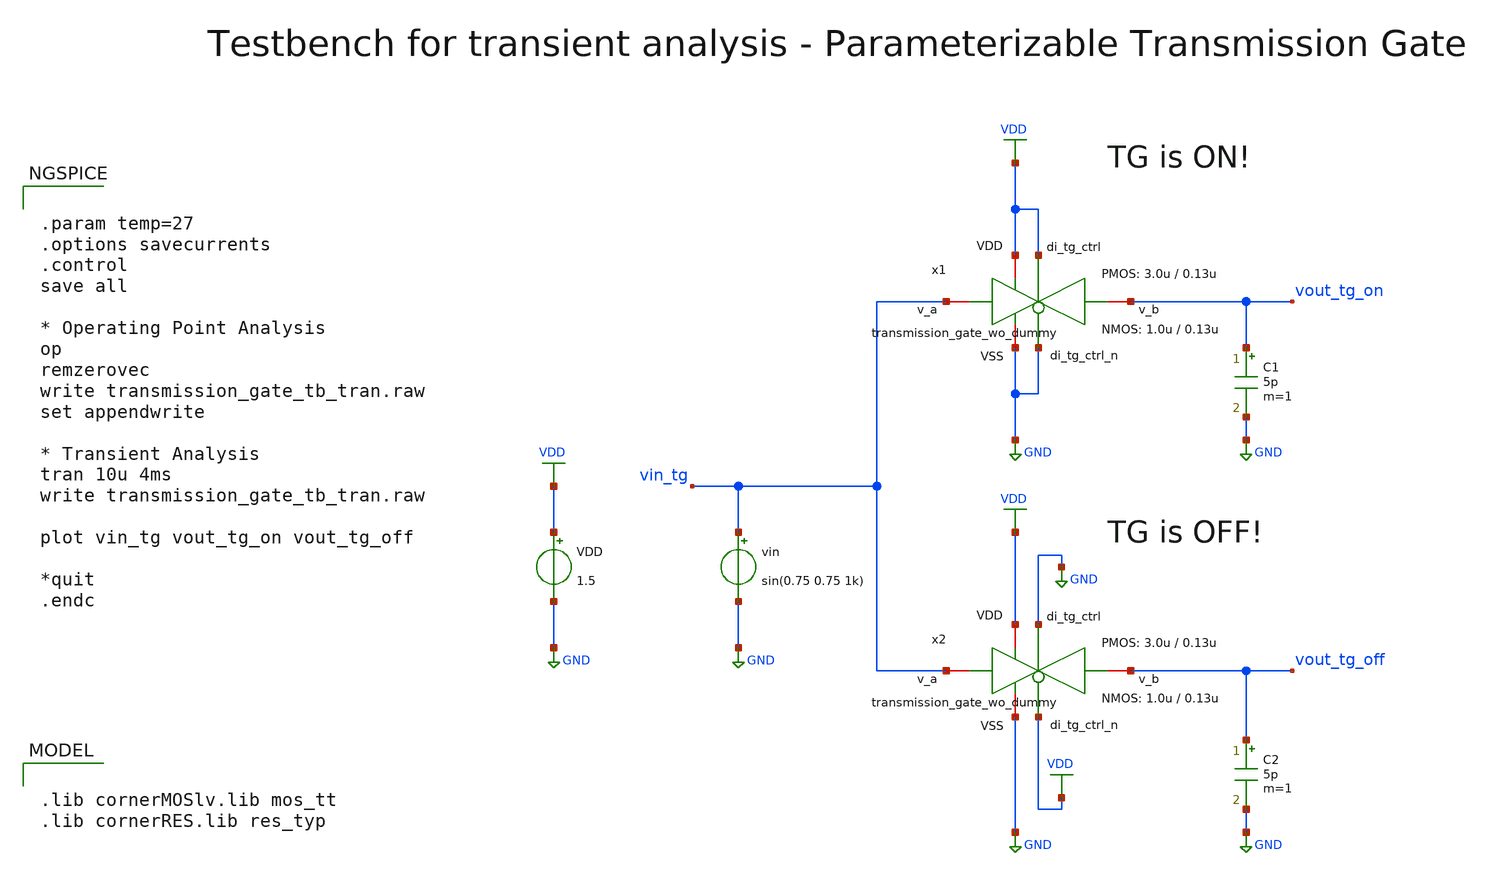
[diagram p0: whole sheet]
** sch_path: xschem/transmission_gate/testbenches/transmission_gate_tb_tran.sch
**.subckt transmission_gate_tb_tran
VDD VDD GND 1.5
vin vin_tg GND sin(0.75 0.75 1k)
C1 vout_tg_on GND 5p m=1
C2 vout_tg_off GND 5p m=1
x1 VDD VDD GND vout_tg_on vin_tg GND transmission_gate_wo_dummy W_P=3.0u L_P=0.13u W_N=1.0u
+ L_N=0.13u
x2 VDD GND GND vout_tg_off vin_tg VDD transmission_gate_wo_dummy W_P=3.0u L_P=0.13u W_N=1.0u
+ L_N=0.13u
**** begin user architecture code

.lib cornerMOSlv.lib mos_tt
.lib cornerRES.lib res_typ



.param temp=27
.options savecurrents
.control
save all

* Operating Point Analysis
op
remzerovec
write transmission_gate_tb_tran.raw
set appendwrite

* Transient Analysis
tran 10u 4ms
write transmission_gate_tb_tran.raw

plot vin_tg vout_tg_on vout_tg_off

*quit
.endc

**** end user architecture code
**.ends

* expanding   symbol:  transmission_gate/transmission_gate_wo_dummy.sym # of pins=6
** sym_path: xschem/transmission_gate/transmission_gate_wo_dummy.sym
** sch_path: xschem/transmission_gate/transmission_gate_wo_dummy.sch
.subckt transmission_gate_wo_dummy VDD di_tg_ctrl VSS v_b v_a di_tg_ctrl_n  W_P=3.0u L_P=0.13u
+ W_N=1.0u L_N=0.13u
*.iopin v_a
*.iopin v_b
*.iopin VDD
*.iopin VSS
*.ipin di_tg_ctrl
*.ipin di_tg_ctrl_n
XM1 v_b di_tg_ctrl v_a VSS sg13_lv_nmos w=W_N l=L_N ng=1 m=1 mm_ok=1
XM2 v_a di_tg_ctrl_n v_b VDD sg13_lv_pmos w=W_P l=L_P ng=1 m=1 mm_ok=1
.ends

.GLOBAL GND
.GLOBAL VDD
.end
